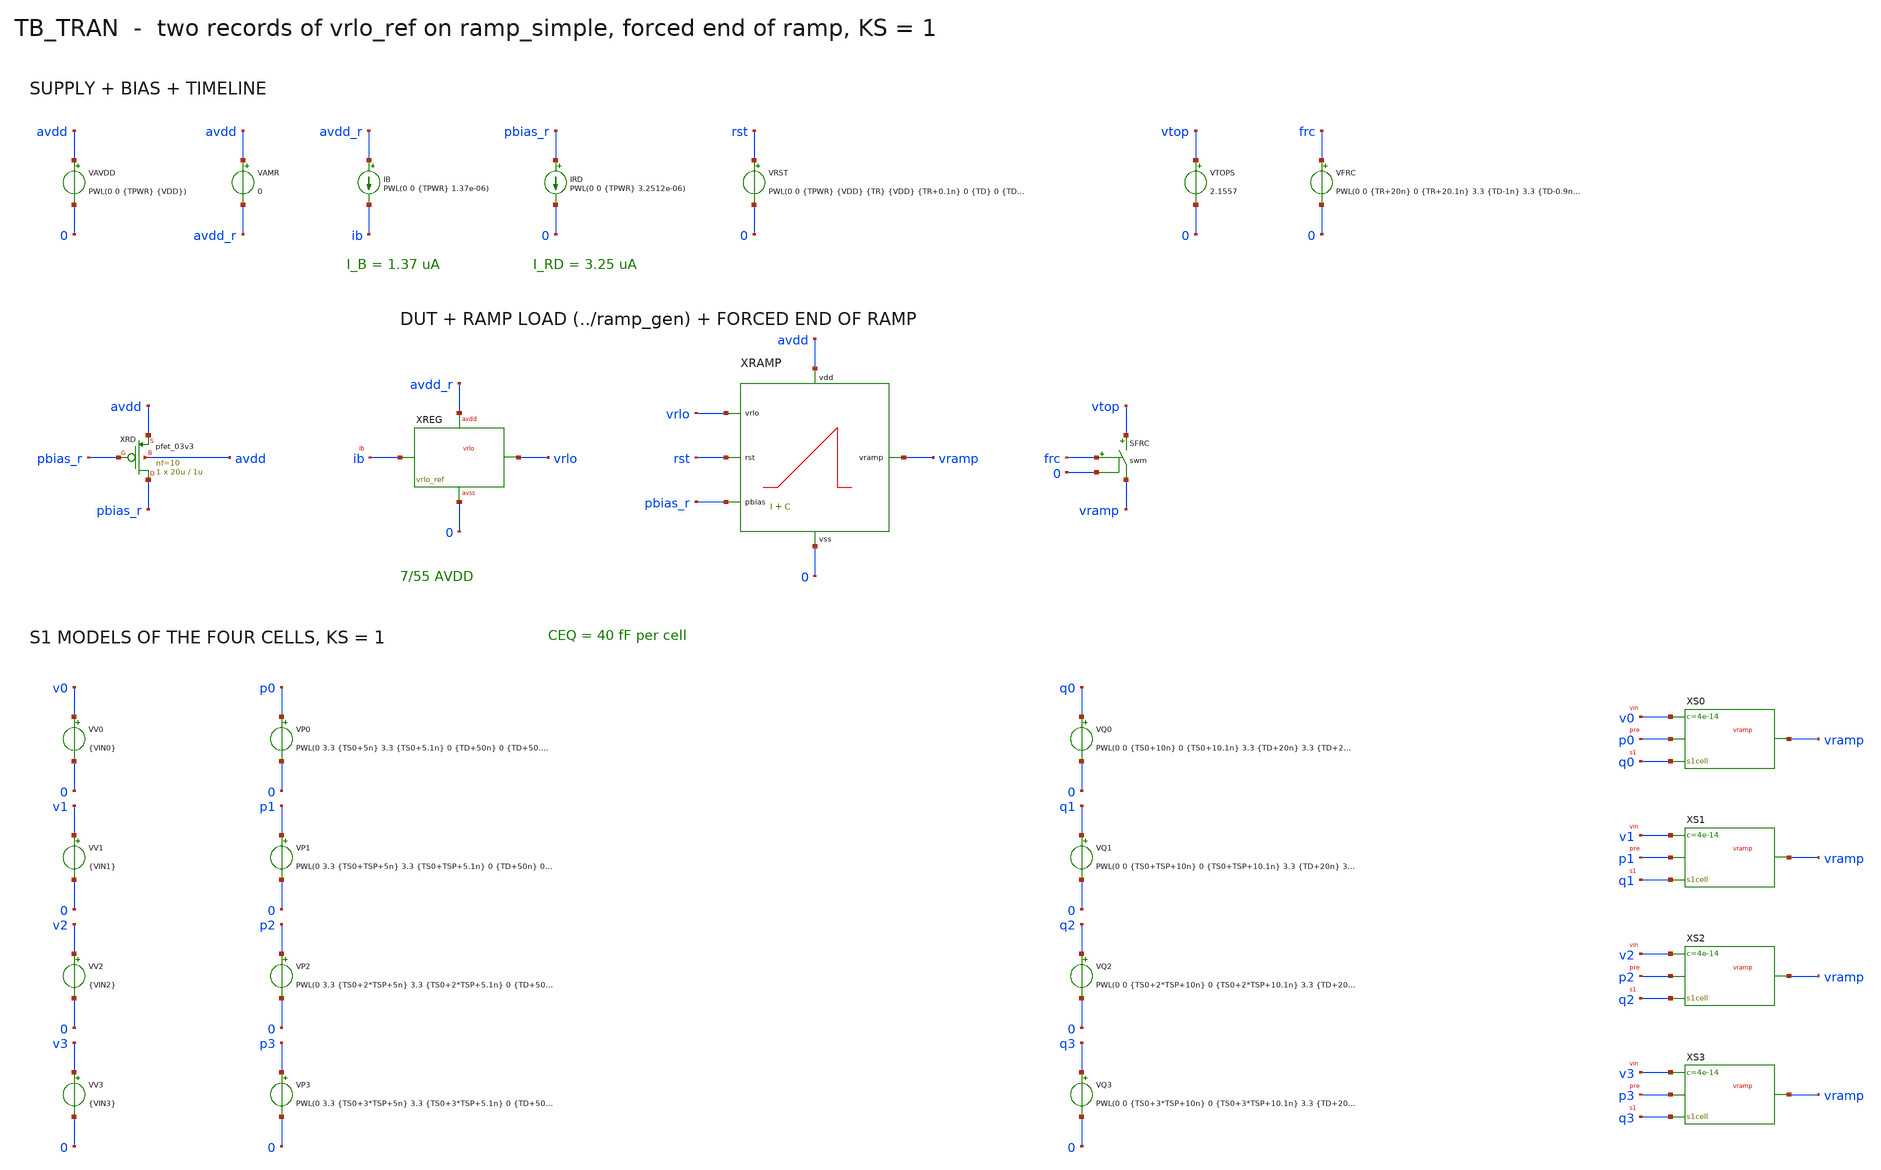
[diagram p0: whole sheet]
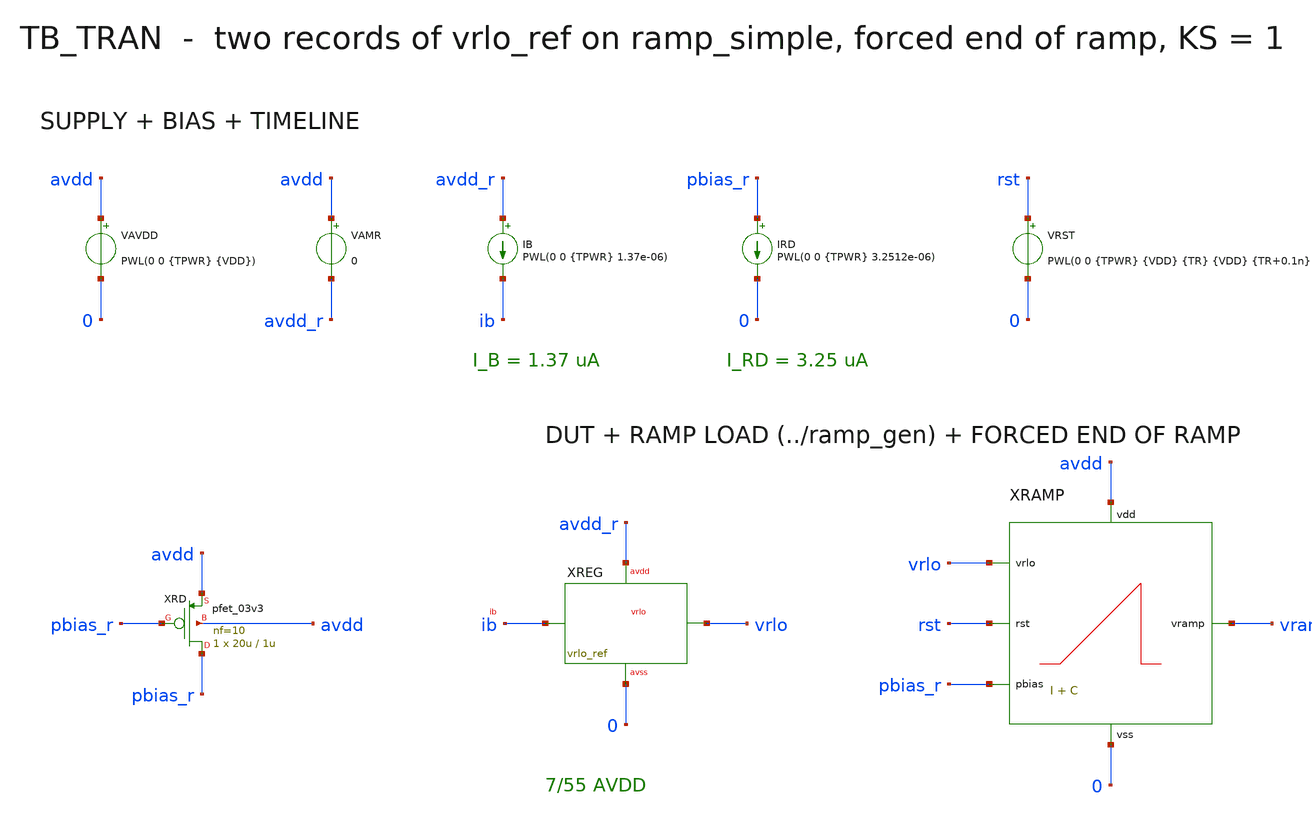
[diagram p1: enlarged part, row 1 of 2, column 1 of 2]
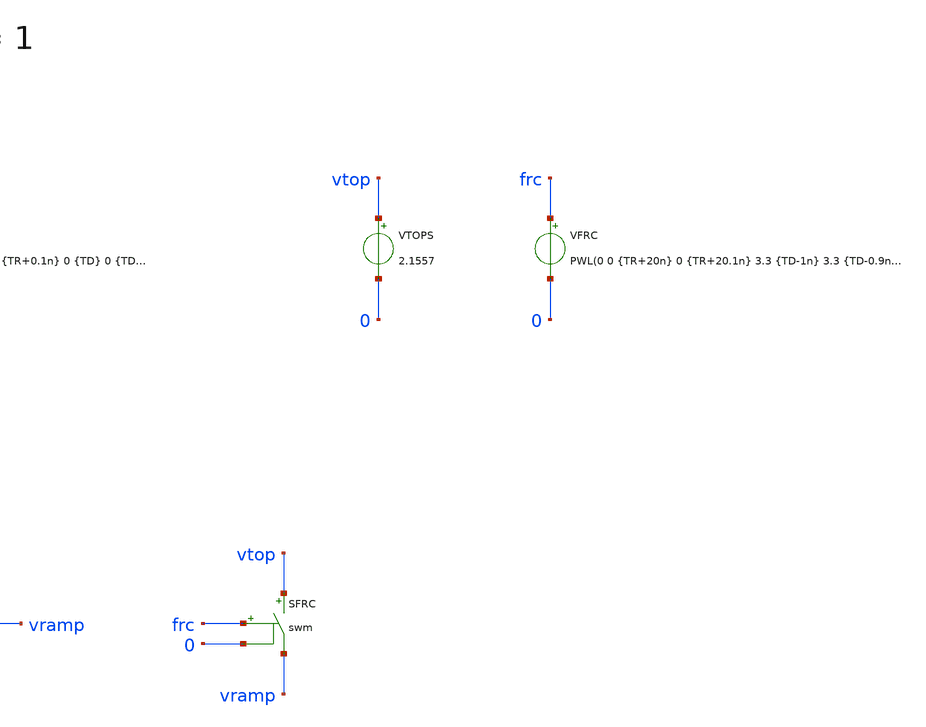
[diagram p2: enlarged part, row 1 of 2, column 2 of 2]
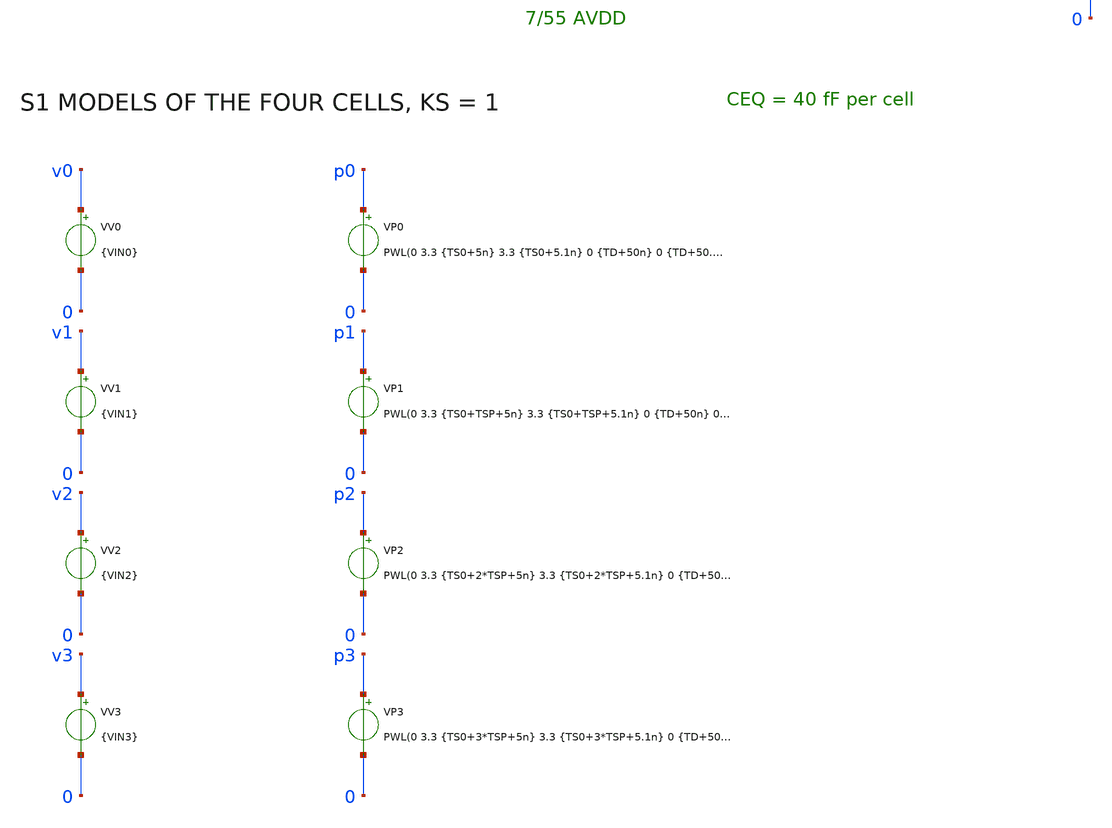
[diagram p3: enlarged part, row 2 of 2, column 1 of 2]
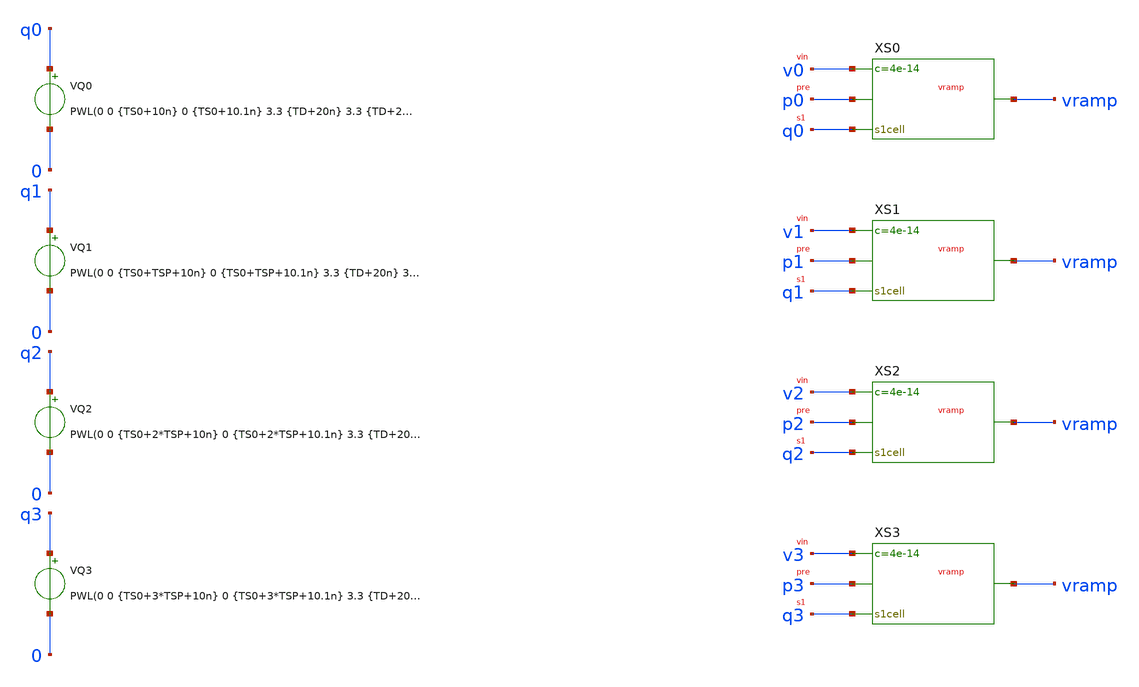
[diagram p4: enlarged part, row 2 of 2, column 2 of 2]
** sch_path: mixed_signal/vrlo_ref/tb_tran.sch
**.subckt tb_tran
VAVDD avdd 0 PWL(0 0 {TPWR} {VDD})
VAMR avdd avdd_r 0
IB avdd_r ib PWL(0 0 {TPWR} 1.37e-06)
XREG vrlo ib avdd_r 0 vrlo_ref
IRD pbias_r 0 PWL(0 0 {TPWR} 3.2512e-06)
XRD pbias_r pbias_r avdd avdd pfet_03v3 L=1u W=20u nf=10 m=1
VRST rst 0 PWL(0 0 {TPWR} {VDD} {TR} {VDD} {TR+0.1n} 0 {TD} 0 {TD+0.1n} {VDD})
XRAMP vramp rst vrlo pbias_r avdd 0 ramp_simple
VTOPS vtop 0 2.1557
VFRC frc 0 PWL(0 0 {TR+20n} 0 {TR+20.1n} 3.3 {TD-1n} 3.3 {TD-0.9n} 0)
SFRC vtop vramp frc 0 swm
VP0 p0 0 PWL(0 3.3 {TS0+5n} 3.3 {TS0+5.1n} 0 {TD+50n} 0 {TD+50.1n} 3.3 {TS0B+5n} 3.3 {TS0B+5.1n} 0)
VP1 p1 0 PWL(0 3.3 {TS0+TSP+5n} 3.3 {TS0+TSP+5.1n} 0 {TD+50n} 0 {TD+50.1n} 3.3 {TS0B+TSP+5n} 3.3 {TS0B+TSP+5.1n}
+ 0)
VP2 p2 0 PWL(0 3.3 {TS0+2*TSP+5n} 3.3 {TS0+2*TSP+5.1n} 0 {TD+50n} 0 {TD+50.1n} 3.3 {TS0B+2*TSP+5n} 3.3
+ {TS0B+2*TSP+5.1n} 0)
VP3 p3 0 PWL(0 3.3 {TS0+3*TSP+5n} 3.3 {TS0+3*TSP+5.1n} 0 {TD+50n} 0 {TD+50.1n} 3.3 {TS0B+3*TSP+5n} 3.3
+ {TS0B+3*TSP+5.1n} 0)
VQ0 q0 0 PWL(0 0 {TS0+10n} 0 {TS0+10.1n} 3.3 {TD+20n} 3.3 {TD+20.1n} 0 {TS0B+10n} 0 {TS0B+10.1n} 3.3)
VQ1 q1 0 PWL(0 0 {TS0+TSP+10n} 0 {TS0+TSP+10.1n} 3.3 {TD+20n} 3.3 {TD+20.1n} 0 {TS0B+TSP+10n} 0 {TS0B+TSP+10.1n}
+ 3.3)
VQ2 q2 0 PWL(0 0 {TS0+2*TSP+10n} 0 {TS0+2*TSP+10.1n} 3.3 {TD+20n} 3.3 {TD+20.1n} 0 {TS0B+2*TSP+10n} 0
+ {TS0B+2*TSP+10.1n} 3.3)
VQ3 q3 0 PWL(0 0 {TS0+3*TSP+10n} 0 {TS0+3*TSP+10.1n} 3.3 {TD+20n} 3.3 {TD+20.1n} 0 {TS0B+3*TSP+10n} 0
+ {TS0B+3*TSP+10.1n} 3.3)
VV0 v0 0 {VIN0}
VV1 v1 0 {VIN1}
VV2 v2 0 {VIN2}
VV3 v3 0 {VIN3}
XS0 vramp v0 p0 q0 s1cell c=4e-14
XS1 vramp v1 p1 q1 s1cell c=4e-14
XS2 vramp v2 p2 q2 s1cell c=4e-14
XS3 vramp v3 p3 q3 s1cell c=4e-14
**** begin user architecture code

.include /foss/pdks/gf180mcuD/libs.tech/ngspice/design.ngspice
.lib /foss/pdks/gf180mcuD/libs.tech/ngspice/sm141064.ngspice typical
.lib /foss/pdks/gf180mcuD/libs.tech/ngspice/sm141064.ngspice res_typical
.lib /foss/pdks/gf180mcuD/libs.tech/ngspice/sm141064.ngspice mimcap_typical
.include /foss/designs/mixed_signal/ramp_gen/data/ramp_simple_params.spice
.temp 27
.param TGAP=300n
.param VDD=3.3 TPWR=100n T0=1e-05 TS0='T0+300n' TSP=40n TR='TS0+3*TSP+TGAP'
.param TD='TR+1.5u' TREC=1e-06 TS0B='TD+TREC' TR2='TS0B+3*TSP+TGAP' TSTOP='TR2+20n'
.param KS=1 VLO='0.1272727273*VDD' DV='1.5/256'
.param VIN0='VLO+KS*16.5*DV' VIN1='VLO+KS*80.5*DV' VIN2='VLO+KS*160.5*DV' VIN3='VLO+KS*240.5*DV'
.model swm sw vt=1.65 vh=0.1 ron=1k roff=1e14
.subckt s1cell vramp vin pre s1 c=40f
SP b vin pre 0 swm
SS b vramp s1 0 swm
CB b 0 {c}
.ends
.options reltol=1e-5 gmin=1e-15
.tran 0.2n {TSTOP} 0 2n
.measure tran vp_q FIND v(vramp) AT={TS0-1n}
.measure tran vp_q2 FIND v(vramp) AT={TS0B-1n}
.measure tran vp_t0 FIND v(vramp) AT={T0}
.measure tran vp_t2u FIND v(vramp) AT=2u
.measure tran vp_tr FIND v(vramp) AT={TR-0.2n}
.measure tran vp_tr2 FIND v(vramp) AT={TR2-0.2n}
.measure tran vr_q FIND v(vrlo) AT={TS0-1n}
.measure tran vtap_q FIND v(xreg.tap) AT={TS0-1n}
.measure tran vg_q FIND v(xreg.g) AT={TS0-1n}
.measure tran vr_frc FIND v(vrlo) AT={TD-1n}
.measure tran vp_td FIND v(vramp) AT={TD-2n}
.measure tran vr_pk MAX v(vrlo) FROM={TD} TO={TS0B}
.measure tran vp_kpk MAX v(vramp) FROM={TS0} TO={TR}
.measure tran ireg_q AVG i(VAMR) FROM={TS0-200n} TO={TS0-10n}
.measure tran ireg_r AVG i(VAMR) FROM={TD-500n} TO={TD-10n}
.control
set num_threads=1
run
quit
.endc

**** end user architecture code
**.ends
.end
